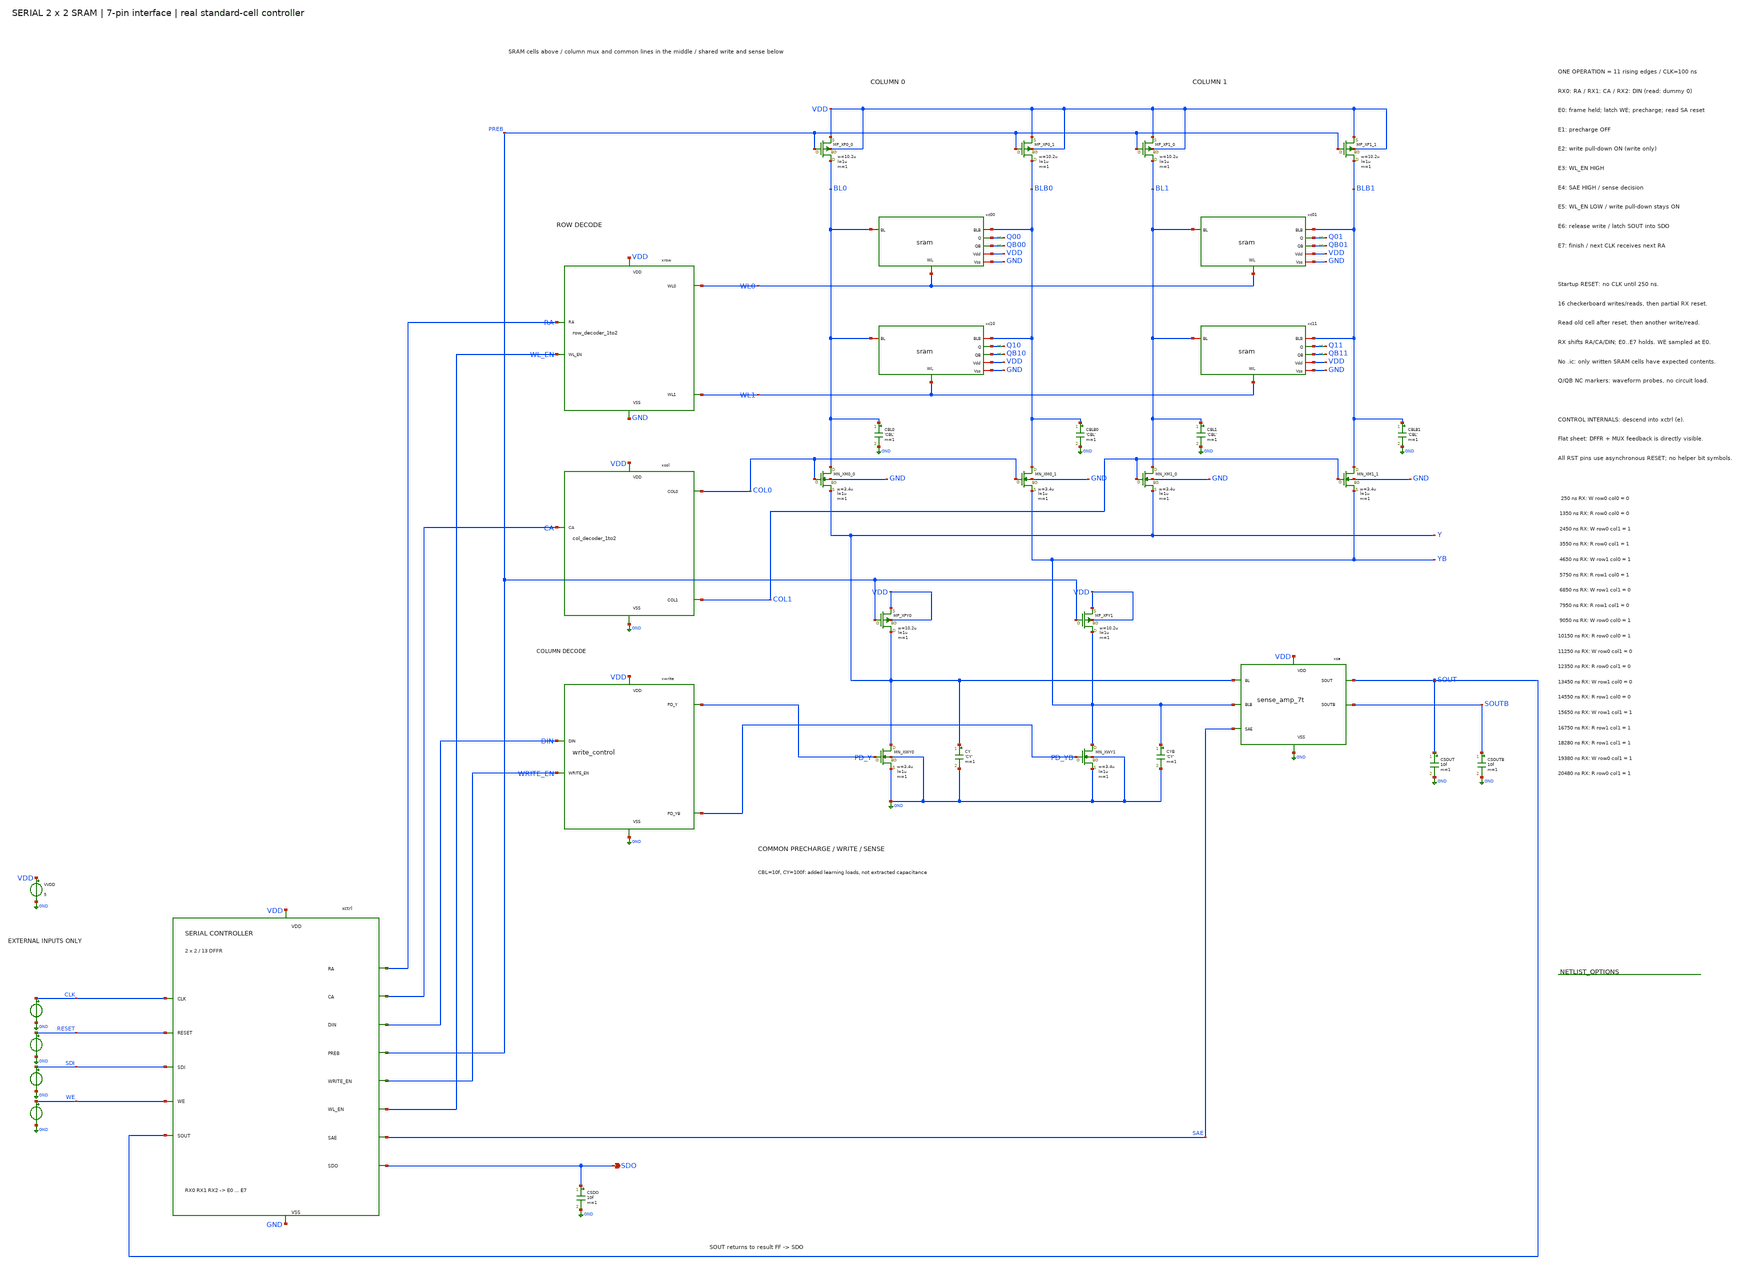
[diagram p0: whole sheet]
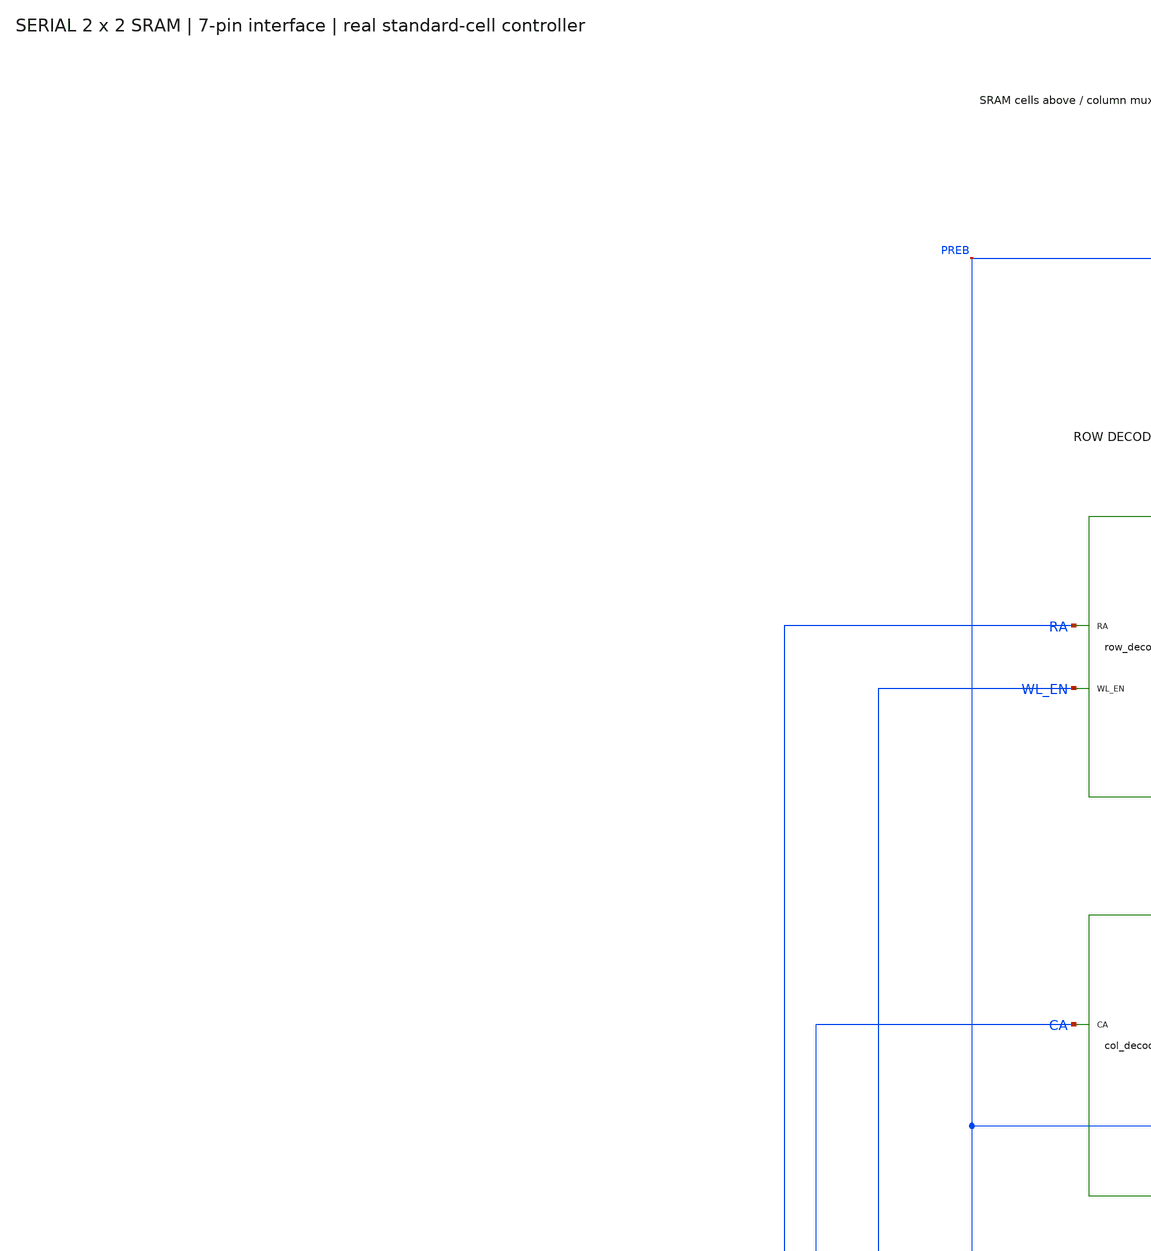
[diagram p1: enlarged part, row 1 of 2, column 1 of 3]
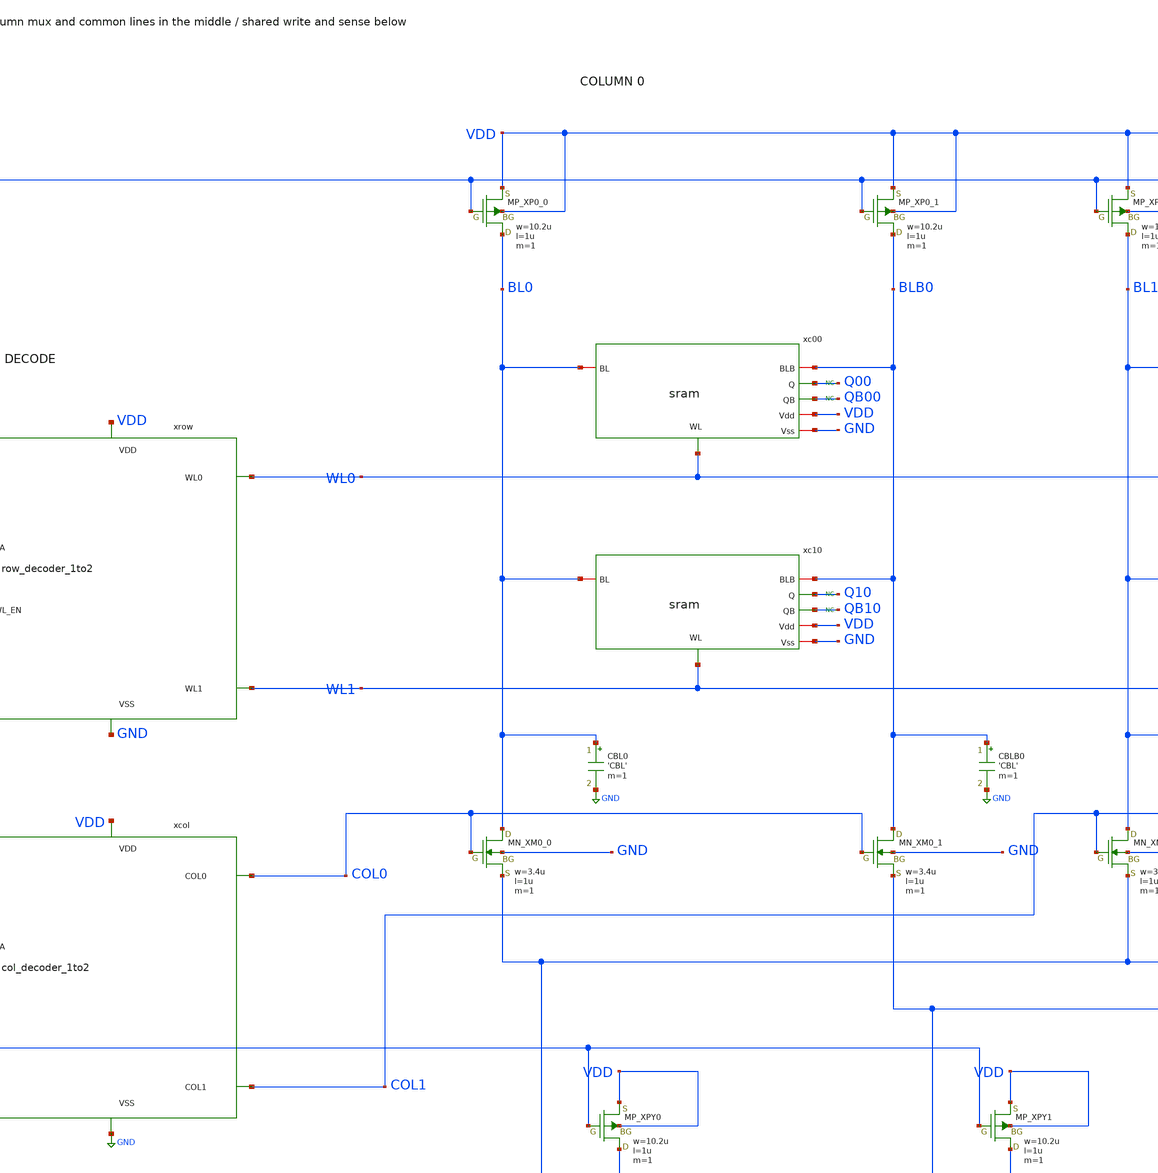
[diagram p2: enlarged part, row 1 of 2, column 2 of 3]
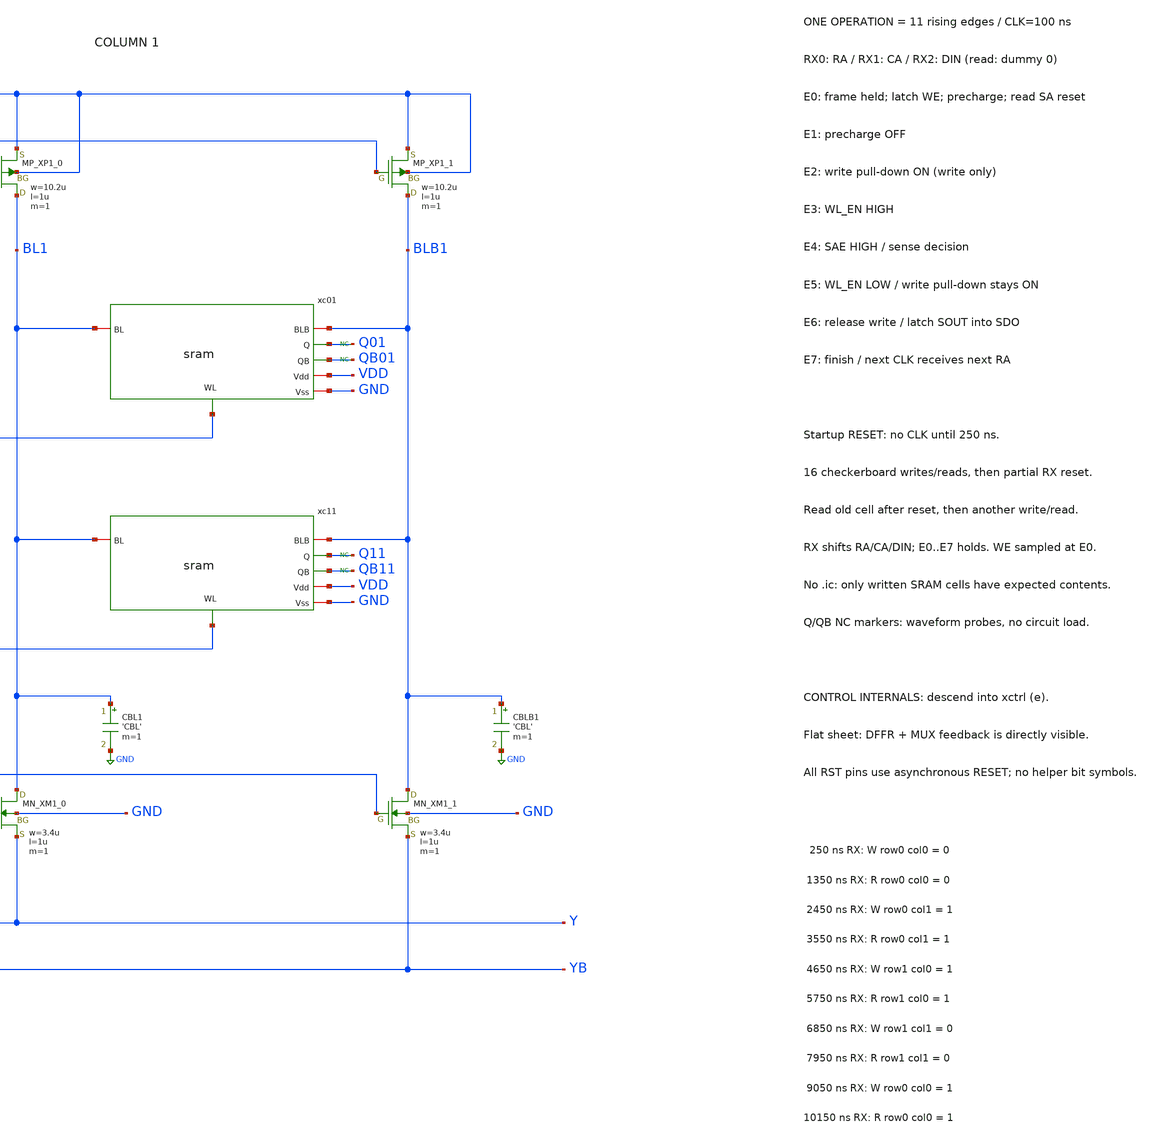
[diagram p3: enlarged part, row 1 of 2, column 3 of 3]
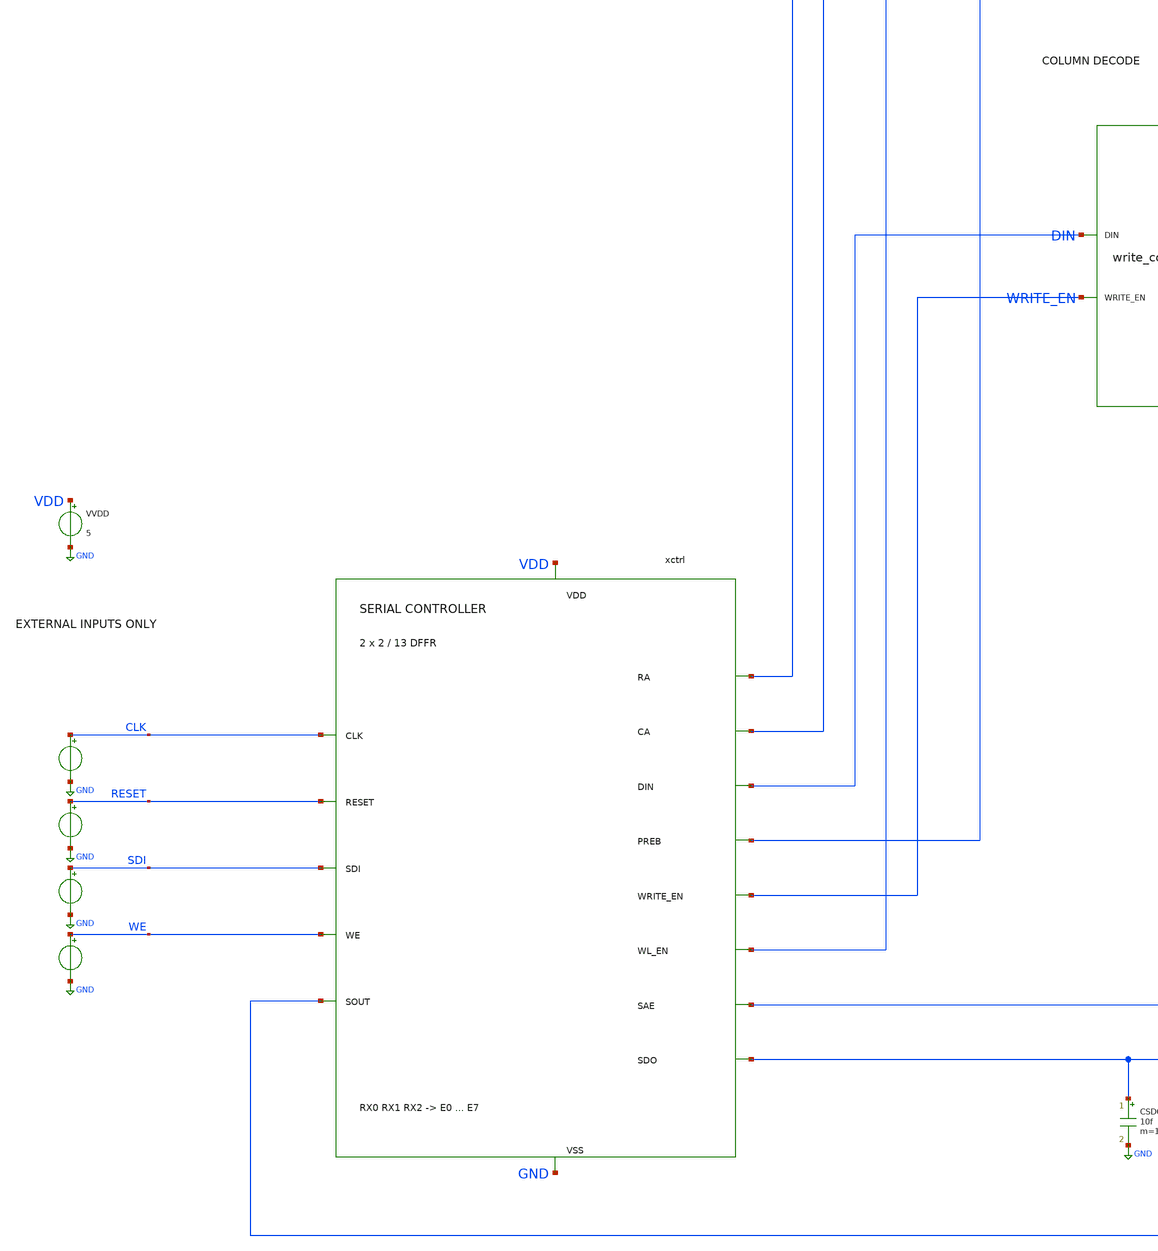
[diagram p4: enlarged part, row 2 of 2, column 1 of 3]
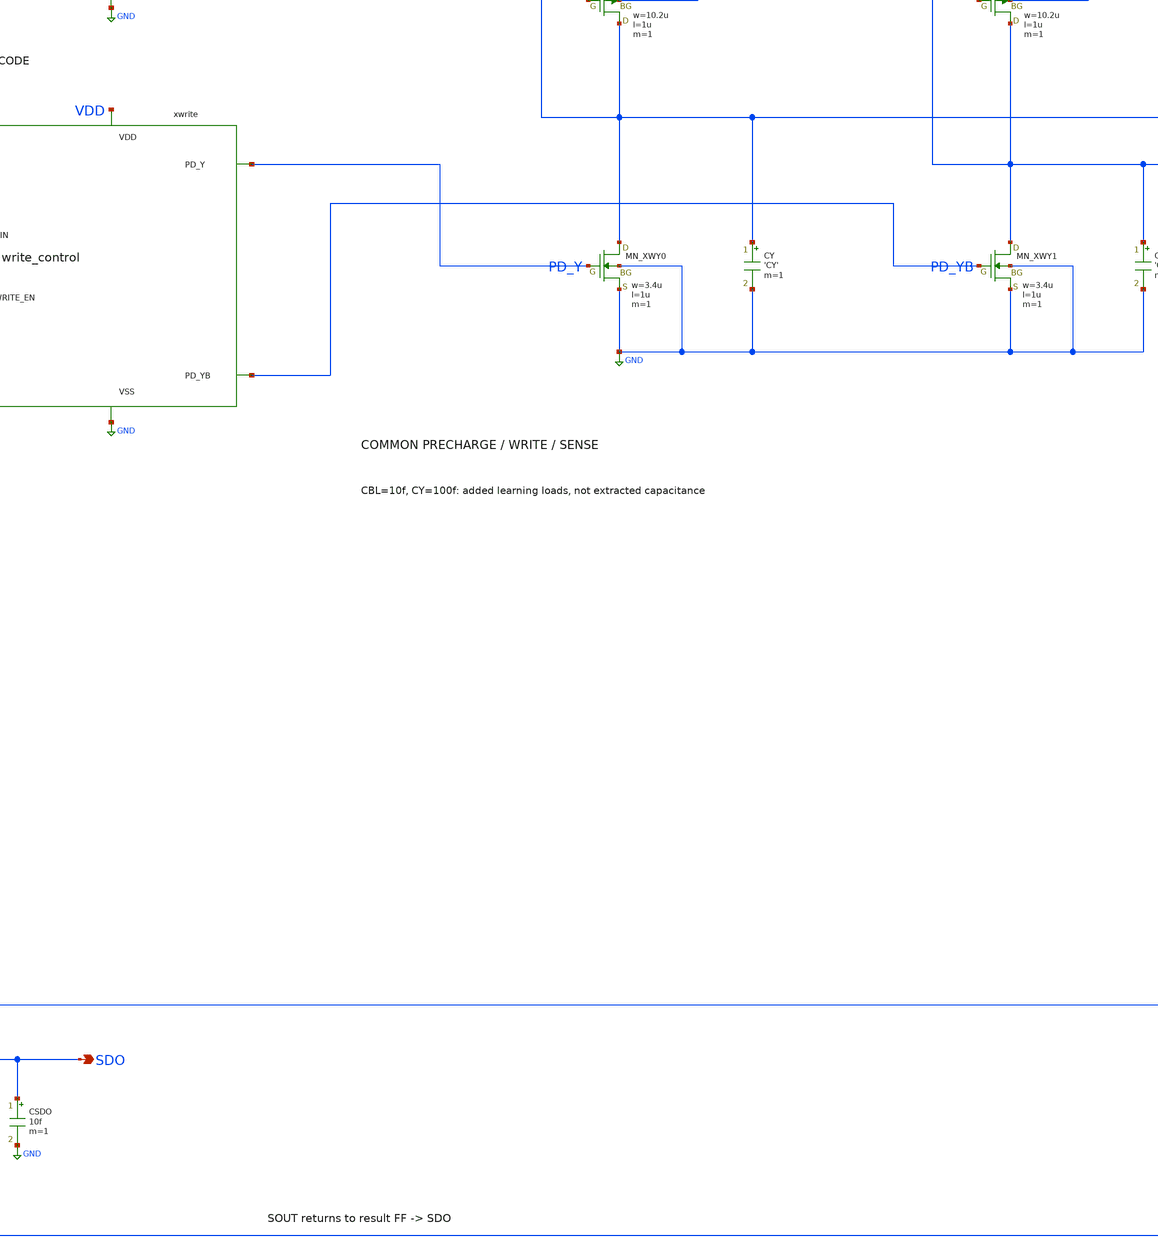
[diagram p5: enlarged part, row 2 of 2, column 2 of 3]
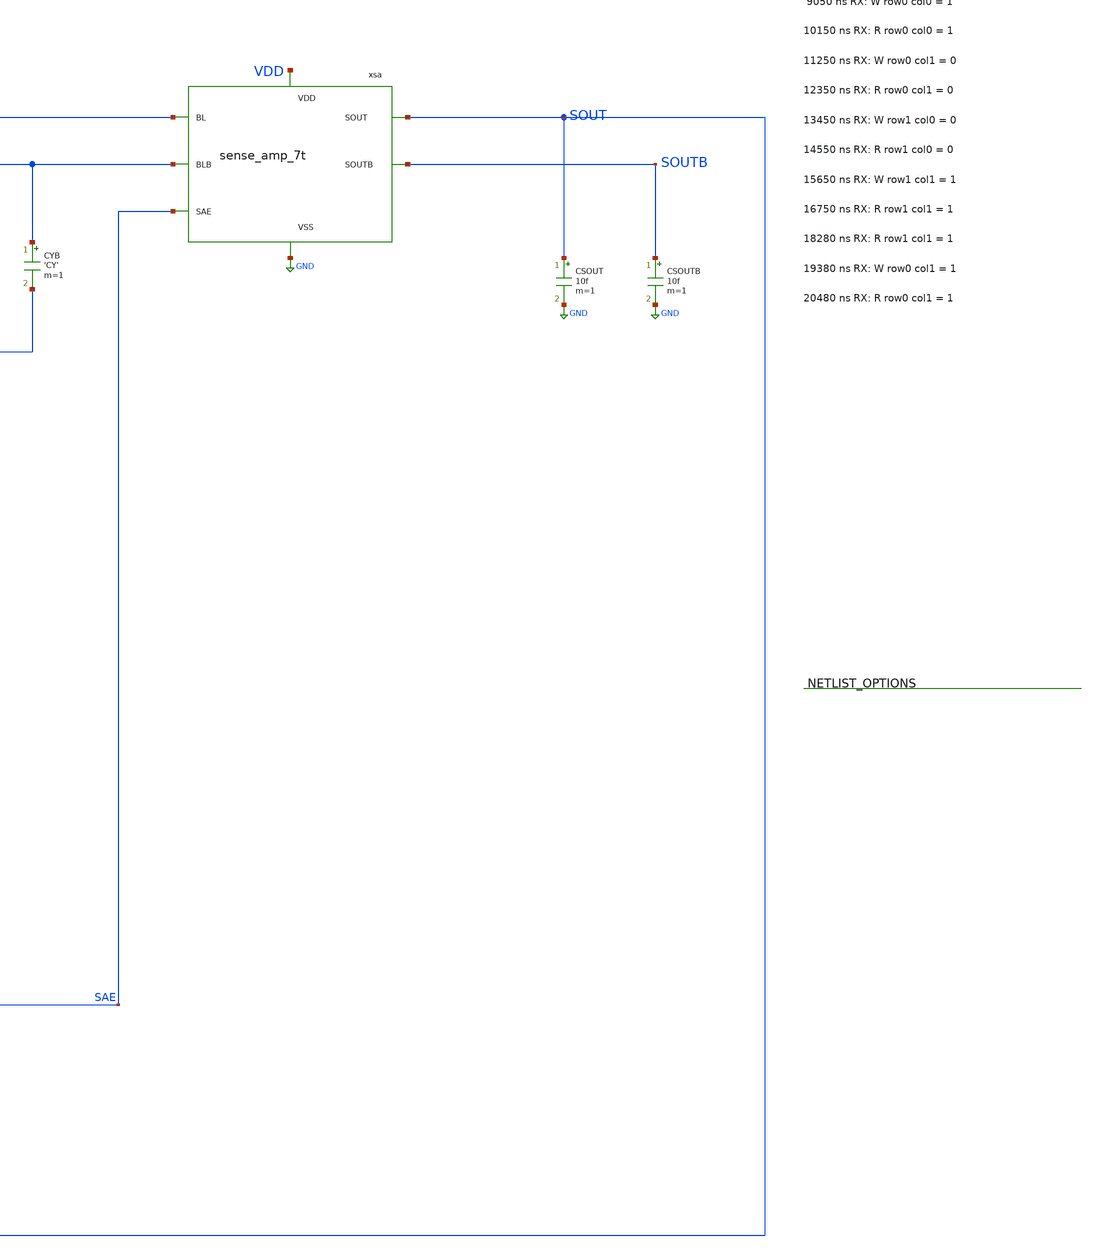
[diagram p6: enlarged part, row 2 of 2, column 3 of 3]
** sch_path: member_project/SRAM/PenguinEino/learning/schematics/sram_tb_serial.sch
**.subckt sram_tb_serial SDO
*.opin SDO
XXP0_0 BL0 PREB VDD VDD PMOS w=10.2u l=1u nrd=0 nrs=0 m=1
CBL0 BL0 GND 'CBL' m=1
XXM0_0 BL0 COL0 Y GND NMOS w=3.4u l=1u nrd=0 nrs=0 m=1
XXP0_1 BLB0 PREB VDD VDD PMOS w=10.2u l=1u nrd=0 nrs=0 m=1
CBLB0 BLB0 GND 'CBL' m=1
XXM0_1 BLB0 COL0 YB GND NMOS w=3.4u l=1u nrd=0 nrs=0 m=1
xc00 WL0 VDD BLB0 Q00 QB00 BL0 GND sram
* noconn Q00
* noconn QB00
xc10 WL1 VDD BLB0 Q10 QB10 BL0 GND sram
* noconn Q10
* noconn QB10
XXP1_0 BL1 PREB VDD VDD PMOS w=10.2u l=1u nrd=0 nrs=0 m=1
CBL1 BL1 GND 'CBL' m=1
XXM1_0 BL1 COL1 Y GND NMOS w=3.4u l=1u nrd=0 nrs=0 m=1
XXP1_1 BLB1 PREB VDD VDD PMOS w=10.2u l=1u nrd=0 nrs=0 m=1
CBLB1 BLB1 GND 'CBL' m=1
XXM1_1 BLB1 COL1 YB GND NMOS w=3.4u l=1u nrd=0 nrs=0 m=1
xc01 WL0 VDD BLB1 Q01 QB01 BL1 GND sram
* noconn Q01
* noconn QB01
xc11 WL1 VDD BLB1 Q11 QB11 BL1 GND sram
* noconn Q11
* noconn QB11
XXPY0 Y PREB VDD VDD PMOS w=10.2u l=1u nrd=0 nrs=0 m=1
XXWY0 Y PD_Y GND GND NMOS w=3.4u l=1u nrd=0 nrs=0 m=1
CY Y GND 'CY' m=1
XXPY1 YB PREB VDD VDD PMOS w=10.2u l=1u nrd=0 nrs=0 m=1
XXWY1 YB PD_YB GND GND NMOS w=3.4u l=1u nrd=0 nrs=0 m=1
CYB YB GND 'CY' m=1
xsa Y YB SAE SOUT SOUTB VDD GND sense_amp_7t
CSOUT SOUT GND 10f m=1
CSOUTB SOUTB GND 10f m=1
xrow RA WL_EN WL0 WL1 VDD GND row_decoder_1to2
xcol CA COL0 COL1 VDD GND col_decoder_1to2
xwrite DIN WRITE_EN PD_Y PD_YB VDD GND write_control
xctrl CLK RESET SDI WE SOUT RA CA DIN PREB WRITE_EN WL_EN SAE SDO VDD GND sram_serial_controller
CSDO SDO GND 10f m=1
VCLK CLK GND PWL(0n 0 250n 0 251n 5 300n 5 301n 0 350n 0 351n 5 400n 5 401n 0 450n 0 451n 5 500n 5
+ 501n 0 550n 0 551n 5 600n 5 601n 0 650n 0 651n 5 700n 5 701n 0 750n 0 751n 5 800n 5 801n 0 850n 0 851n 5
+ 900n 5 901n 0 950n 0 951n 5 1000n 5 1001n 0 1050n 0 1051n 5 1100n 5 1101n 0 1150n 0 1151n 5 1200n 5
+ 1201n 0 1250n 0 1251n 5 1300n 5 1301n 0 1350n 0 1351n 5 1400n 5 1401n 0 1450n 0 1451n 5 1500n 5 1501n 0
+ 1550n 0 1551n 5 1600n 5 1601n 0 1650n 0 1651n 5 1700n 5 1701n 0 1750n 0 1751n 5 1800n 5 1801n 0 1850n 0
+ 1851n 5 1900n 5 1901n 0 1950n 0 1951n 5 2000n 5 2001n 0 2050n 0 2051n 5 2100n 5 2101n 0 2150n 0 2151n 5
+ 2200n 5 2201n 0 2250n 0 2251n 5 2300n 5 2301n 0 2350n 0 2351n 5 2400n 5 2401n 0 2450n 0 2451n 5 2500n 5
+ 2501n 0 2550n 0 2551n 5 2600n 5 2601n 0 2650n 0 2651n 5 2700n 5 2701n 0 2750n 0 2751n 5 2800n 5 2801n 0
+ 2850n 0 2851n 5 2900n 5 2901n 0 2950n 0 2951n 5 3000n 5 3001n 0 3050n 0 3051n 5 3100n 5 3101n 0 3150n 0
+ 3151n 5 3200n 5 3201n 0 3250n 0 3251n 5 3300n 5 3301n 0 3350n 0 3351n 5 3400n 5 3401n 0 3450n 0 3451n 5
+ 3500n 5 3501n 0 3550n 0 3551n 5 3600n 5 3601n 0 3650n 0 3651n 5 3700n 5 3701n 0 3750n 0 3751n 5 3800n 5
+ 3801n 0 3850n 0 3851n 5 3900n 5 3901n 0 3950n 0 3951n 5 4000n 5 4001n 0 4050n 0 4051n 5 4100n 5 4101n 0
+ 4150n 0 4151n 5 4200n 5 4201n 0 4250n 0 4251n 5 4300n 5 4301n 0 4350n 0 4351n 5 4400n 5 4401n 0 4450n 0
+ 4451n 5 4500n 5 4501n 0 4550n 0 4551n 5 4600n 5 4601n 0 4650n 0 4651n 5 4700n 5 4701n 0 4750n 0 4751n 5
+ 4800n 5 4801n 0 4850n 0 4851n 5 4900n 5 4901n 0 4950n 0 4951n 5 5000n 5 5001n 0 5050n 0 5051n 5 5100n 5
+ 5101n 0 5150n 0 5151n 5 5200n 5 5201n 0 5250n 0 5251n 5 5300n 5 5301n 0 5350n 0 5351n 5 5400n 5 5401n 0
+ 5450n 0 5451n 5 5500n 5 5501n 0 5550n 0 5551n 5 5600n 5 5601n 0 5650n 0 5651n 5 5700n 5 5701n 0 5750n 0
+ 5751n 5 5800n 5 5801n 0 5850n 0 5851n 5 5900n 5 5901n 0 5950n 0 5951n 5 6000n 5 6001n 0 6050n 0 6051n 5
+ 6100n 5 6101n 0 6150n 0 6151n 5 6200n 5 6201n 0 6250n 0 6251n 5 6300n 5 6301n 0 6350n 0 6351n 5 6400n 5
+ 6401n 0 6450n 0 6451n 5 6500n 5 6501n 0 6550n 0 6551n 5 6600n 5 6601n 0 6650n 0 6651n 5 6700n 5 6701n 0
+ 6750n 0 6751n 5 6800n 5 6801n 0 6850n 0 6851n 5 6900n 5 6901n 0 6950n 0 6951n 5 7000n 5 7001n 0 7050n 0
+ 7051n 5 7100n 5 7101n 0 7150n 0 7151n 5 7200n 5 7201n 0 7250n 0 7251n 5 7300n 5 7301n 0 7350n 0 7351n 5
+ 7400n 5 7401n 0 7450n 0 7451n 5 7500n 5 7501n 0 7550n 0 7551n 5 7600n 5 7601n 0 7650n 0 7651n 5 7700n 5
+ 7701n 0 7750n 0 7751n 5 7800n 5 7801n 0 7850n 0 7851n 5 7900n 5 7901n 0 7950n 0 7951n 5 8000n 5 8001n 0
+ 8050n 0 8051n 5 8100n 5 8101n 0 8150n 0 8151n 5 8200n 5 8201n 0 8250n 0 8251n 5 8300n 5 8301n 0 8350n 0
+ 8351n 5 8400n 5 8401n 0 8450n 0 8451n 5 8500n 5 8501n 0 8550n 0 8551n 5 8600n 5 8601n 0 8650n 0 8651n 5
+ 8700n 5 8701n 0 8750n 0 8751n 5 8800n 5 8801n 0 8850n 0 8851n 5 8900n 5 8901n 0 8950n 0 8951n 5 9000n 5
+ 9001n 0 9050n 0 9051n 5 9100n 5 9101n 0 9150n 0 9151n 5 9200n 5 9201n 0 9250n 0 9251n 5 9300n 5 9301n 0
+ 9350n 0 9351n 5 9400n 5 9401n 0 9450n 0 9451n 5 9500n 5 9501n 0 9550n 0 9551n 5 9600n 5 9601n 0 9650n 0
+ 9651n 5 9700n 5 9701n 0 9750n 0 9751n 5 9800n 5 9801n 0 9850n 0 9851n 5 9900n 5 9901n 0 9950n 0 9951n 5
+ 10000n 5 10001n 0 10050n 0 10051n 5 10100n 5 10101n 0 10150n 0 10151n 5 10200n 5 10201n 0 10250n 0 10251n
+ 5 10300n 5 10301n 0 10350n 0 10351n 5 10400n 5 10401n 0 10450n 0 10451n 5 10500n 5 10501n 0 10550n 0
+ 10551n 5 10600n 5 10601n 0 10650n 0 10651n 5 10700n 5 10701n 0 10750n 0 10751n 5 10800n 5 10801n 0 10850n
+ 0 10851n 5 10900n 5 10901n 0 10950n 0 10951n 5 11000n 5 11001n 0 11050n 0 11051n 5 11100n 5 11101n 0
+ 11150n 0 11151n 5 11200n 5 11201n 0 11250n 0 11251n 5 11300n 5 11301n 0 11350n 0 11351n 5 11400n 5 11401n
+ 0 11450n 0 11451n 5 11500n 5 11501n 0 11550n 0 11551n 5 11600n 5 11601n 0 11650n 0 11651n 5 11700n 5
+ 11701n 0 11750n 0 11751n 5 11800n 5 11801n 0 11850n 0 11851n 5 11900n 5 11901n 0 11950n 0 11951n 5 12000n
+ 5 12001n 0 12050n 0 12051n 5 12100n 5 12101n 0 12150n 0 12151n 5 12200n 5 12201n 0 12250n 0 12251n 5
+ 12300n 5 12301n 0 12350n 0 12351n 5 12400n 5 12401n 0 12450n 0 12451n 5 12500n 5 12501n 0 12550n 0 12551n
+ 5 12600n 5 12601n 0 12650n 0 12651n 5 12700n 5 12701n 0 12750n 0 12751n 5 12800n 5 12801n 0 12850n 0
+ 12851n 5 12900n 5 12901n 0 12950n 0 12951n 5 13000n 5 13001n 0 13050n 0 13051n 5 13100n 5 13101n 0 13150n
+ 0 13151n 5 13200n 5 13201n 0 13250n 0 13251n 5 13300n 5 13301n 0 13350n 0 13351n 5 13400n 5 13401n 0
+ 13450n 0 13451n 5 13500n 5 13501n 0 13550n 0 13551n 5 13600n 5 13601n 0 13650n 0 13651n 5 13700n 5 13701n
+ 0 13750n 0 13751n 5 13800n 5 13801n 0 13850n 0 13851n 5 13900n 5 13901n 0 13950n 0 13951n 5 14000n 5
+ 14001n 0 14050n 0 14051n 5 14100n 5 14101n 0 14150n 0 14151n 5 14200n 5 14201n 0 14250n 0 14251n 5 14300n
+ 5 14301n 0 14350n 0 14351n 5 14400n 5 14401n 0 14450n 0 14451n 5 14500n 5 14501n 0 14550n 0 14551n 5
+ 14600n 5 14601n 0 14650n 0 14651n 5 14700n 5 14701n 0 14750n 0 14751n 5 14800n 5 14801n 0 14850n 0 14851n
+ 5 14900n 5 14901n 0 14950n 0 14951n 5 15000n 5 15001n 0 15050n 0 15051n 5 15100n 5 15101n 0 15150n 0
+ 15151n 5 15200n 5 15201n 0 15250n 0 15251n 5 15300n 5 15301n 0 15350n 0 15351n 5 15400n 5 15401n 0 15450n
+ 0 15451n 5 15500n 5 15501n 0 15550n 0 15551n 5 15600n 5 15601n 0 15650n 0 15651n 5 15700n 5 15701n 0
+ 15750n 0 15751n 5 15800n 5 15801n 0 15850n 0 15851n 5 15900n 5 15901n 0 15950n 0 15951n 5 16000n 5 16001n
+ 0 16050n 0 16051n 5 16100n 5 16101n 0 16150n 0 16151n 5 16200n 5 16201n 0 16250n 0 16251n 5 16300n 5
+ 16301n 0 16350n 0 16351n 5 16400n 5 16401n 0 16450n 0 16451n 5 16500n 5 16501n 0 16550n 0 16551n 5 16600n
+ 5 16601n 0 16650n 0 16651n 5 16700n 5 16701n 0 16750n 0 16751n 5 16800n 5 16801n 0 16850n 0 16851n 5
+ 16900n 5 16901n 0 16950n 0 16951n 5 17000n 5 17001n 0 17050n 0 17051n 5 17100n 5 17101n 0 17150n 0 17151n
+ 5 17200n 5 17201n 0 17250n 0 17251n 5 17300n 5 17301n 0 17350n 0 17351n 5 17400n 5 17401n 0 17450n 0
+ 17451n 5 17500n 5 17501n 0 17550n 0 17551n 5 17600n 5 17601n 0 17650n 0 17651n 5 17700n 5 17701n 0 17750n
+ 0 17751n 5 17800n 5 17801n 0 17850n 0 17851n 5 17900n 5 17901n 0 17950n 0 17951n 5 18000n 5 18001n 0
+ 18280n 0 18281n 5 18330n 5 18331n 0 18380n 0 18381n 5 18430n 5 18431n 0 18480n 0 18481n 5 18530n 5 18531n
+ 0 18580n 0 18581n 5 18630n 5 18631n 0 18680n 0 18681n 5 18730n 5 18731n 0 18780n 0 18781n 5 18830n 5
+ 18831n 0 18880n 0 18881n 5 18930n 5 18931n 0 18980n 0 18981n 5 19030n 5 19031n 0 19080n 0 19081n 5 19130n
+ 5 19131n 0 19180n 0 19181n 5 19230n 5 19231n 0 19280n 0 19281n 5 19330n 5 19331n 0 19380n 0 19381n 5
+ 19430n 5 19431n 0 19480n 0 19481n 5 19530n 5 19531n 0 19580n 0 19581n 5 19630n 5 19631n 0 19680n 0 19681n
+ 5 19730n 5 19731n 0 19780n 0 19781n 5 19830n 5 19831n 0 19880n 0 19881n 5 19930n 5 19931n 0 19980n 0
+ 19981n 5 20030n 5 20031n 0 20080n 0 20081n 5 20130n 5 20131n 0 20180n 0 20181n 5 20230n 5 20231n 0 20280n
+ 0 20281n 5 20330n 5 20331n 0 20380n 0 20381n 5 20430n 5 20431n 0 20480n 0 20481n 5 20530n 5 20531n 0
+ 20580n 0 20581n 5 20630n 5 20631n 0 20680n 0 20681n 5 20730n 5 20731n 0 20780n 0 20781n 5 20830n 5 20831n
+ 0 20880n 0 20881n 5 20930n 5 20931n 0 20980n 0 20981n 5 21030n 5 21031n 0 21080n 0 21081n 5 21130n 5
+ 21131n 0 21180n 0 21181n 5 21230n 5 21231n 0 21280n 0 21281n 5 21330n 5 21331n 0 21380n 0 21381n 5 21430n
+ 5 21431n 0 21480n 0 21481n 5 21530n 5 21531n 0 21680n 0)
VRESET RESET GND PWL(0n 5 120n 5 121n 0 18030n 0 18031n 5 18160n 5 18161n 0 21680n 0)
VSDI SDI GND PWL(0n 0 610n 0 611n 5 710n 5 711n 0 810n 0 811n 5 910n 5 911n 0 1010n 0 1011n 5 1110n
+ 5 1111n 0 1210n 0 1211n 5 1310n 5 1311n 0 1710n 0 1711n 5 1810n 5 1811n 0 1910n 0 1911n 5 2010n 5
+ 2011n 0 2110n 0 2111n 5 2210n 5 2211n 0 2310n 0 2311n 5 2410n 5 2411n 0 2510n 0 2511n 5 2710n 5 2711n 0
+ 2810n 0 2811n 5 2910n 5 2911n 0 3010n 0 3011n 5 3110n 5 3111n 0 3210n 0 3211n 5 3310n 5 3311n 0 3410n 0
+ 3411n 5 3510n 5 3511n 0 3610n 0 3611n 5 3710n 5 3711n 0 3910n 0 3911n 5 4010n 5 4011n 0 4110n 0 4111n 5
+ 4210n 5 4211n 0 4310n 0 4311n 5 4410n 5 4411n 0 4510n 0 4511n 5 4710n 5 4711n 0 4810n 0 4811n 5 4910n 5
+ 4911n 0 5010n 0 5011n 5 5110n 5 5111n 0 5210n 0 5211n 5 5310n 5 5311n 0 5410n 0 5411n 5 5510n 5 5511n 0
+ 5610n 0 5611n 5 5810n 5 5811n 0 6110n 0 6111n 5 6210n 5 6211n 0 6310n 0 6311n 5 6410n 5 6411n 0 6510n 0
+ 6511n 5 6610n 5 6611n 0 6710n 0 6711n 5 7010n 5 7011n 0 7210n 0 7211n 5 7310n 5 7311n 0 7410n 0 7411n 5
+ 7510n 5 7511n 0 7610n 0 7611n 5 7710n 5 7711n 0 7810n 0 7811n 5 8110n 5 8111n 0 8310n 0 8311n 5 8410n 5
+ 8411n 0 8510n 0 8511n 5 8610n 5 8611n 0 8710n 0 8711n 5 8810n 5 8811n 0 8910n 0 8911n 5 9010n 5 9011n 0
+ 9210n 0 9211n 5 9310n 5 9311n 0 9410n 0 9411n 5 9510n 5 9511n 0 9610n 0 9611n 5 9710n 5 9711n 0 9810n 0
+ 9811n 5 9910n 5 9911n 0 10010n 0 10011n 5 10110n 5 10111n 0 10510n 0 10511n 5 10610n 5 10611n 0 10710n 0
+ 10711n 5 10810n 5 10811n 0 10910n 0 10911n 5 11010n 5 11011n 0 11110n 0 11111n 5 11210n 5 11211n 0 11310n
+ 0 11311n 5 11410n 5 11411n 0 11610n 0 11611n 5 11710n 5 11711n 0 11810n 0 11811n 5 11910n 5 11911n 0
+ 12010n 0 12011n 5 12110n 5 12111n 0 12210n 0 12211n 5 12310n 5 12311n 0 12410n 0 12411n 5 12510n 5 12511n
+ 0 12710n 0 12711n 5 12810n 5 12811n 0 12910n 0 12911n 5 13010n 5 13011n 0 13110n 0 13111n 5 13210n 5
+ 13211n 0 13310n 0 13311n 5 13510n 5 13511n 0 13810n 0 13811n 5 13910n 5 13911n 0 14010n 0 14011n 5 14110n
+ 5 14111n 0 14210n 0 14211n 5 14310n 5 14311n 0 14410n 0 14411n 5 14610n 5 14611n 0 14910n 0 14911n 5
+ 15010n 5 15011n 0 15110n 0 15111n 5 15210n 5 15211n 0 15310n 0 15311n 5 15410n 5 15411n 0 15510n 0 15511n
+ 5 15910n 5 15911n 0 16010n 0 16011n 5 16110n 5 16111n 0 16210n 0 16211n 5 16310n 5 16311n 0 16410n 0
+ 16411n 5 16510n 5 16511n 0 16610n 0 16611n 5 16910n 5 16911n 0 17110n 0 17111n 5 17210n 5 17211n 0 17310n
+ 0 17311n 5 17410n 5 17411n 0 17510n 0 17511n 5 17610n 5 17611n 0 17710n 0 17711n 5 18440n 5 18441n 0
+ 18640n 0 18641n 5 18740n 5 18741n 0 18840n 0 18841n 5 18940n 5 18941n 0 19040n 0 19041n 5 19140n 5 19141n
+ 0 19240n 0 19241n 5 19340n 5 19341n 0 19440n 0 19441n 5 19640n 5 19641n 0 19740n 0 19741n 5 19840n 5
+ 19841n 0 19940n 0 19941n 5 20040n 5 20041n 0 20140n 0 20141n 5 20240n 5 20241n 0 20340n 0 20341n 5 20440n
+ 5 20441n 0 20540n 0 20541n 5 20640n 5 20641n 0 20840n 0 20841n 5 20940n 5 20941n 0 21040n 0 21041n 5
+ 21140n 5 21141n 0 21240n 0 21241n 5 21340n 5 21341n 0 21440n 0 21441n 5 21680n 5)
VWE WE GND PWL(0n 0 310n 0 311n 5 410n 5 411n 0 510n 0 511n 5 610n 5 611n 0 1410n 0 1411n 5 1510n 5
+ 1511n 0 1710n 0 1711n 5 2410n 5 2411n 0 2510n 0 2511n 5 2610n 5 2611n 0 2710n 0 2711n 5 2810n 5 2811n 0
+ 3610n 0 3611n 5 3710n 5 3711n 0 3910n 0 3911n 5 4610n 5 4611n 0 4710n 0 4711n 5 4810n 5 4811n 0 4910n 0
+ 4911n 5 5010n 5 5011n 0 5810n 0 5811n 5 5910n 5 5911n 0 6110n 0 6111n 5 6810n 5 6811n 0 6910n 0 6911n 5
+ 7010n 5 7011n 0 7110n 0 7111n 5 7210n 5 7211n 0 8010n 0 8011n 5 8110n 5 8111n 0 8310n 0 8311n 5 9010n 5
+ 9011n 0 9110n 0 9111n 5 9210n 5 9211n 0 9310n 0 9311n 5 9410n 5 9411n 0 10210n 0 10211n 5 10310n 5 10311n
+ 0 10510n 0 10511n 5 11210n 5 11211n 0 11310n 0 11311n 5 11410n 5 11411n 0 11510n 0 11511n 5 11610n 5
+ 11611n 0 12410n 0 12411n 5 12510n 5 12511n 0 12710n 0 12711n 5 13410n 5 13411n 0 13510n 0 13511n 5 13610n
+ 5 13611n 0 13710n 0 13711n 5 13810n 5 13811n 0 14610n 0 14611n 5 14710n 5 14711n 0 14910n 0 14911n 5
+ 15610n 5 15611n 0 15710n 0 15711n 5 15810n 5 15811n 0 15910n 0 15911n 5 16010n 5 16011n 0 16810n 0 16811n
+ 5 16910n 5 16911n 0 17110n 0 17111n 5 17810n 5 17811n 0 18340n 0 18341n 5 18440n 5 18441n 0 18640n 0
+ 18641n 5 19340n 5 19341n 0 19440n 0 19441n 5 19540n 5 19541n 0 19640n 0 19641n 5 19740n 5 19741n 0 20540n
+ 0 20541n 5 20640n 5 20641n 0 20840n 0 20841n 5 21680n 5)
VVDD VDD GND 5
**** begin user architecture code
 .include $::LIB/ip62_models

.param CBL=10f CY=100f
.control
save v(CLK) v(RESET) v(SDI) v(WE) v(SDO) v(RA) v(CA) v(DIN) v(PREB) v(WL_EN) v(WRITE_EN) v(SAE)
+ v(WL0) v(WL1) v(COL0) v(COL1) v(PD_Y) v(PD_YB) v(BL0) v(BLB0) v(BL1) v(BLB1) v(Y) v(YB) v(SOUT) v(SOUTB)
+ v(Q00) v(Q01) v(Q10) v(Q11) v(QB00) v(QB01) v(QB10) v(QB11) v(xctrl.C0) v(xctrl.C1) v(xctrl.C2)
+ v(xctrl.C3) v(xctrl.W) v(xctrl.RX) v(xctrl.E0) v(xctrl.E1) v(xctrl.E2) v(xctrl.E3) v(xctrl.E4) v(xctrl.E5)
+ v(xctrl.E6) v(xctrl.E7)
tran 0.5n 21680n
let failures = 0
meas tran cell0 find v(Q00) at=1330n
if cell0 > 0.5
 let failures = failures + 1
end
meas tran cell1 find v(Q00) at=2430n
if cell1 > 0.5
 let failures = failures + 1
end
meas tran read1 find v(SDO) at=2330n
if read1 > 0.5
 let failures = failures + 1
end
meas tran cell2 find v(Q01) at=3530n
if cell2 < 4.5
 let failures = failures + 1
end
meas tran cell3 find v(Q01) at=4630n
if cell3 < 4.5
 let failures = failures + 1
end
meas tran read3 find v(SDO) at=4530n
if read3 < 4.5
 let failures = failures + 1
end
meas tran cell4 find v(Q10) at=5730n
if cell4 < 4.5
 let failures = failures + 1
end
meas tran cell5 find v(Q10) at=6830n
if cell5 < 4.5
 let failures = failures + 1
end
meas tran read5 find v(SDO) at=6730n
if read5 < 4.5
 let failures = failures + 1
end
meas tran cell6 find v(Q11) at=7930n
if cell6 > 0.5
 let failures = failures + 1
end
meas tran cell7 find v(Q11) at=9030n
if cell7 > 0.5
 let failures = failures + 1
end
meas tran read7 find v(SDO) at=8930n
if read7 > 0.5
 let failures = failures + 1
end
meas tran cell8 find v(Q00) at=10130n
if cell8 < 4.5
 let failures = failures + 1
end
meas tran cell9 find v(Q00) at=11230n
if cell9 < 4.5
 let failures = failures + 1
end
meas tran read9 find v(SDO) at=11130n
if read9 < 4.5
 let failures = failures + 1
end
meas tran cell10 find v(Q01) at=12330n
if cell10 > 0.5
 let failures = failures + 1
end
meas tran cell11 find v(Q01) at=13430n
if cell11 > 0.5
 let failures = failures + 1
end
meas tran read11 find v(SDO) at=13330n
if read11 > 0.5
 let failures = failures + 1
end
meas tran cell12 find v(Q10) at=14530n
if cell12 > 0.5
 let failures = failures + 1
end
meas tran cell13 find v(Q10) at=15630n
if cell13 > 0.5
 let failures = failures + 1
end
meas tran read13 find v(SDO) at=15530n
if read13 > 0.5
 let failures = failures + 1
end
meas tran cell14 find v(Q11) at=16730n
if cell14 < 4.5
 let failures = failures + 1
end
meas tran cell15 find v(Q11) at=17830n
if cell15 < 4.5
 let failures = failures + 1
end
meas tran read15 find v(SDO) at=17730n
if read15 < 4.5
 let failures = failures + 1
end
meas tran cell16 find v(Q11) at=19360n
if cell16 < 4.5
 let failures = failures + 1
end
meas tran read16 find v(SDO) at=19260n
if read16 < 4.5
 let failures = failures + 1
end
meas tran cell17 find v(Q01) at=20460n
if cell17 < 4.5
 let failures = failures + 1
end
meas tran cell18 find v(Q01) at=21560n
if cell18 < 4.5
 let failures = failures + 1
end
meas tran read18 find v(SDO) at=21460n
if read18 < 4.5
 let failures = failures + 1
end
if failures = 0
 echo PASS: serial writes and reads; run scripts/verify_serial_spice.py for RTL and timing checks
else
 echo FAIL: serial SRAM; inspect measurements
 print failures
end
let count = (v(xctrl.C0)+2*v(xctrl.C1)+4*v(xctrl.C2)+8*v(xctrl.C3))/5
set wr_singlescale
set wr_vecnames
wrdata serial_spice_waveforms.txt v(CLK) v(RESET) v(SDI) v(WE) v(SDO) v(RA) v(CA) v(DIN) v(PREB)
+ v(WL_EN) v(WRITE_EN) v(SAE) v(WL0) v(WL1) v(COL0) v(COL1) v(PD_Y) v(PD_YB) v(BL0) v(BLB0) v(BL1) v(BLB1)
+ v(Y) v(YB) v(SOUT) v(SOUTB) v(Q00) v(Q01) v(Q10) v(Q11) v(QB00) v(QB01) v(QB10) v(QB11) v(xctrl.C0)
+ v(xctrl.C1) v(xctrl.C2) v(xctrl.C3) v(xctrl.W) v(xctrl.RX) v(xctrl.E0) v(xctrl.E1) v(xctrl.E2) v(xctrl.E3)
+ v(xctrl.E4) v(xctrl.E5) v(xctrl.E6) v(xctrl.E7)
write sram_tb_serial.raw
plot v(CLK) v(SDI) v(WE) xlimit 180n 1500n title 'SERIAL INPUT: RX at 250 / 350 / 450 ns, E0 at 550 ns'
plot count xlimit 180n 2550n title 'COUNT: 0..10; pre-edge count names the action'
plot v(RA) v(CA) v(DIN) v(xctrl.W) xlimit 180n 2550n title 'FRAME: RA/CA/DIN shift during RX; hold E0..E7; W samples WE at E0'
plot v(SOUT) v(SDO) title 'READ RESULT: SDO captures SOUT at E6 and holds through writes'
plot v(Q00) v(Q01) v(Q10) v(Q11) title 'STORED CELLS: written by serial commands, no initial-value forcing'
let PREB_T = v(PREB)/5+6
let WRITE_EN_T = v(WRITE_EN)/5+4
let WL_EN_T = v(WL_EN)/5+2
let SAE_T = v(SAE)/5+0
plot PREB_T WRITE_EN_T WL_EN_T SAE_T xlimit 450n 2450n title 'CONTROLS: PREB+6 WRITE_EN+4 WL_EN+2 SAE+0'
.endc

**** end user architecture code
**.ends
.GLOBAL GND
.end
